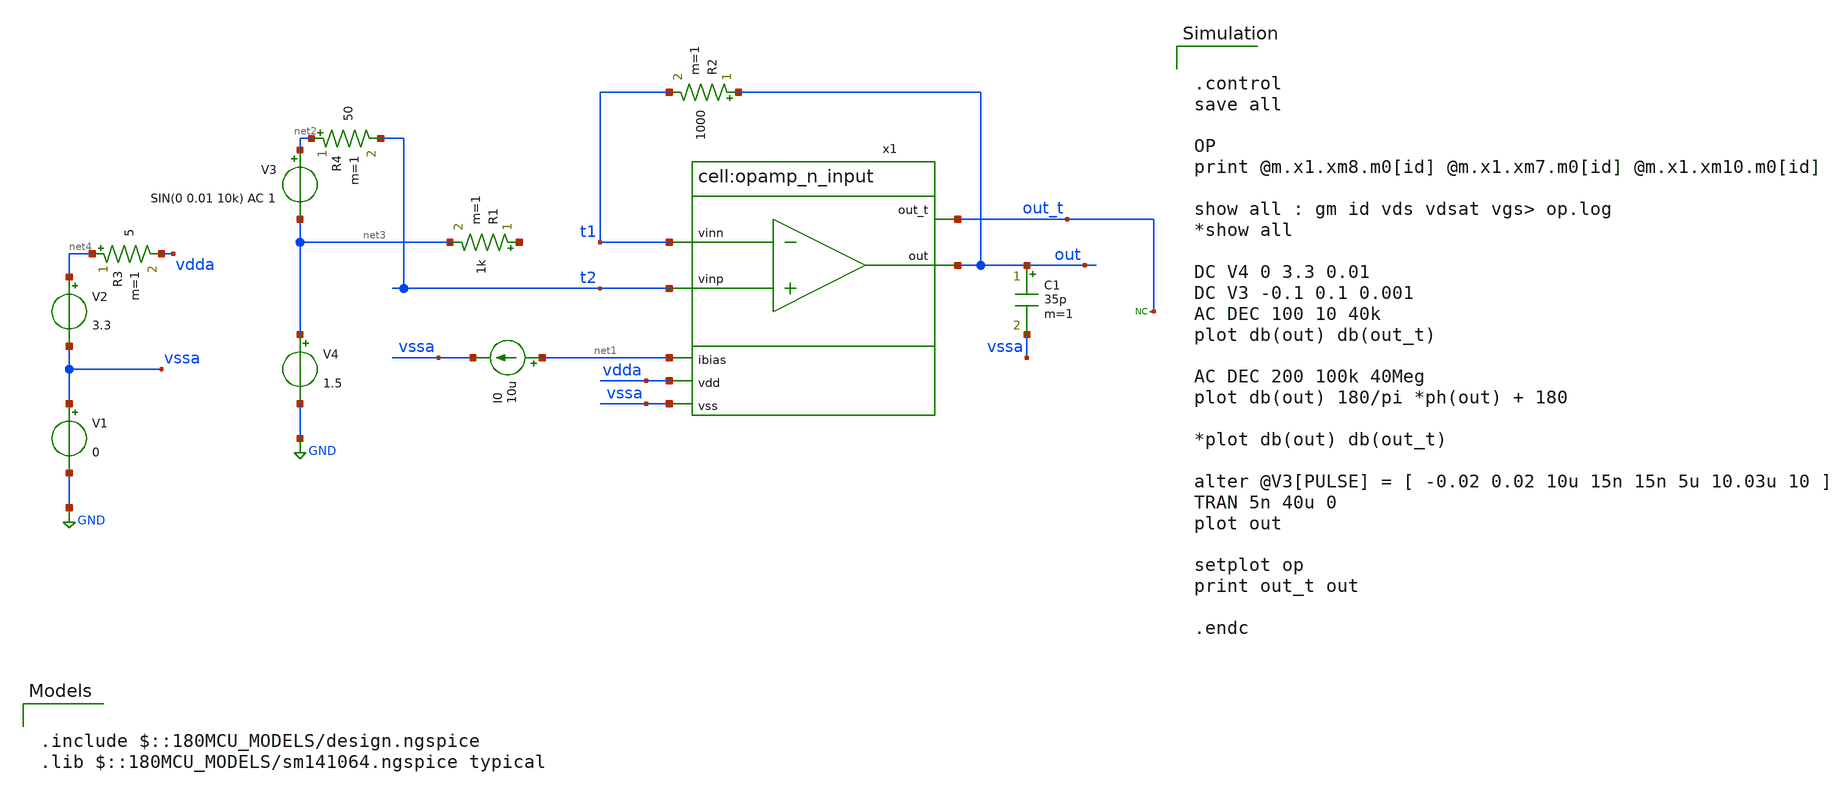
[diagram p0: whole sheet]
** sch_path: designs/libs/tb_analog/opamp/opamp_n_tb.sch
**.subckt opamp_n_tb
x1 t2 t1 net1 vdda out vssa out_t opamp_n_input
V1 vssa GND 0
V2 net4 vssa 3.3
I0 net1 vssa 10u
V3 net2 net3 SIN(0 0.01 10k) AC 1
V4 net3 GND 1.5
C1 out vssa 35p m=1
* noconn out_t
R1 net5 net3 1k m=1
R2 out t1 1000 m=1
R4 net2 t2 50 m=1
R3 net4 vdda 5 m=1
**** begin user architecture code


.control
save all

OP
print @m.x1.xm8.m0[id] @m.x1.xm7.m0[id] @m.x1.xm10.m0[id]

show all : gm id vds vdsat vgs> op.log
*show all

DC V4 0 3.3 0.01
DC V3 -0.1 0.1 0.001
AC DEC 100 10 40k
plot db(out) db(out_t)

AC DEC 200 100k 40Meg
plot db(out) 180/pi *ph(out) + 180

*plot db(out) db(out_t)

alter @V3[PULSE] = [ -0.02 0.02 10u 15n 15n 5u 10.03u 10 ]
TRAN 5n 40u 0
plot out

setplot op
print out_t out

.endc



.include $::180MCU_MODELS/design.ngspice
.lib $::180MCU_MODELS/sm141064.ngspice typical

**** end user architecture code
**.ends
.GLOBAL GND
.end
